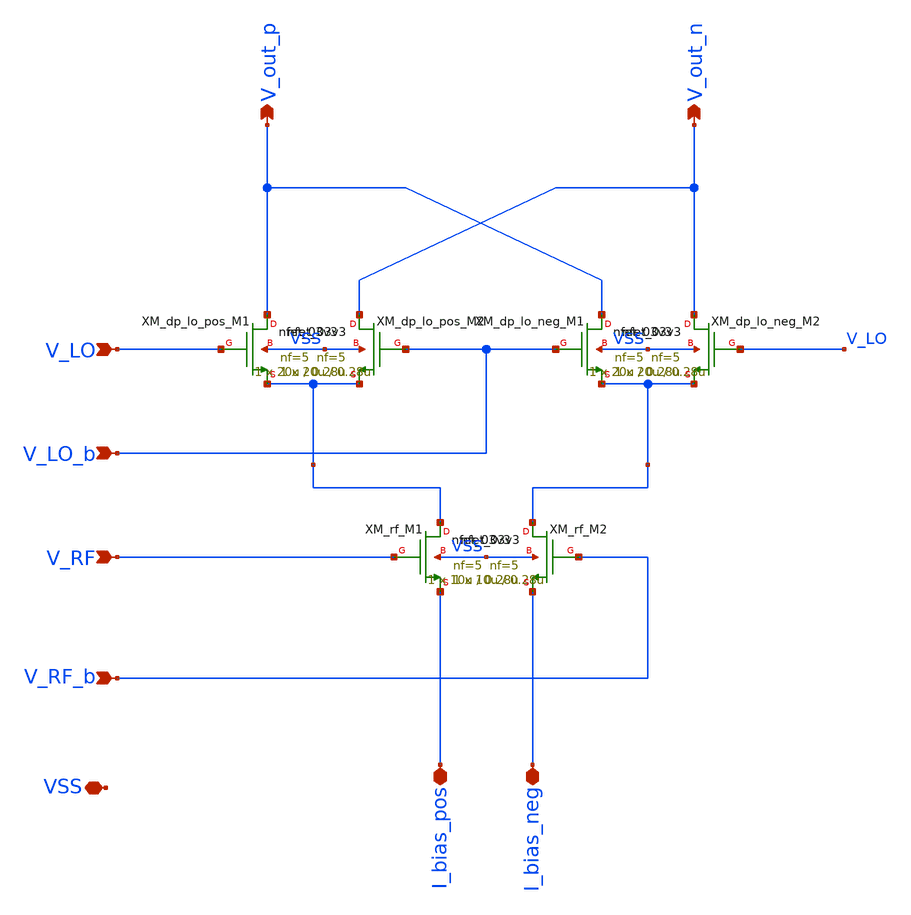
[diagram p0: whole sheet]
** sch_path: src/python/Gilbert_mixer/Gilbert_cell_hierarchal_mixing_stage.sch
**.subckt Gilbert_cell_hierarchal_mixing_stage V_LO V_LO_b V_RF V_RF_b V_out_p V_out_n I_bias_neg
*+ I_bias_pos VSS
*.ipin V_LO
*.ipin V_LO_b
*.ipin V_RF
*.ipin V_RF_b
*.opin V_out_p
*.opin V_out_n
*.iopin I_bias_neg
*.iopin I_bias_pos
*.iopin VSS
XM_dp_lo_pos_M1 V_out_p V_LO rf_diff_pair_pos_input VSS nfet_03v3 L=0.28u W=20u nf=5 ad='int((nf+1)/2) * W/nf * 0.18u'
+ as='int((nf+2)/2) * W/nf * 0.18u' pd='2*int((nf+1)/2) * (W/nf + 0.18u)' ps='2*int((nf+2)/2) * (W/nf + 0.18u)'
+ nrd='0.18u / W' nrs='0.18u / W' sa=0 sb=0 sd=0 m=1
XM_dp_lo_pos_M2 V_out_n V_LO_b rf_diff_pair_pos_input VSS nfet_03v3 L=0.28u W=20u nf=5 ad='int((nf+1)/2) * W/nf * 0.18u'
+ as='int((nf+2)/2) * W/nf * 0.18u' pd='2*int((nf+1)/2) * (W/nf + 0.18u)' ps='2*int((nf+2)/2) * (W/nf + 0.18u)'
+ nrd='0.18u / W' nrs='0.18u / W' sa=0 sb=0 sd=0 m=1
XM_dp_lo_neg_M1 V_out_p V_LO_b rf_diff_pair_neg_input VSS nfet_03v3 L=0.28u W=20u nf=5 ad='int((nf+1)/2) * W/nf * 0.18u'
+ as='int((nf+2)/2) * W/nf * 0.18u' pd='2*int((nf+1)/2) * (W/nf + 0.18u)' ps='2*int((nf+2)/2) * (W/nf + 0.18u)'
+ nrd='0.18u / W' nrs='0.18u / W' sa=0 sb=0 sd=0 m=1
XM_dp_lo_neg_M2 V_out_n V_LO rf_diff_pair_neg_input VSS nfet_03v3 L=0.28u W=20u nf=5 ad='int((nf+1)/2) * W/nf * 0.18u'
+ as='int((nf+2)/2) * W/nf * 0.18u' pd='2*int((nf+1)/2) * (W/nf + 0.18u)' ps='2*int((nf+2)/2) * (W/nf + 0.18u)'
+ nrd='0.18u / W' nrs='0.18u / W' sa=0 sb=0 sd=0 m=1
XM_rf_M1 rf_diff_pair_pos_input V_RF I_bias_pos VSS nfet_03v3 L=0.28u W=10u nf=5 ad='int((nf+1)/2) * W/nf * 0.18u'
+ as='int((nf+2)/2) * W/nf * 0.18u' pd='2*int((nf+1)/2) * (W/nf + 0.18u)' ps='2*int((nf+2)/2) * (W/nf + 0.18u)'
+ nrd='0.18u / W' nrs='0.18u / W' sa=0 sb=0 sd=0 m=1
XM_rf_M2 rf_diff_pair_neg_input V_RF_b I_bias_neg VSS nfet_03v3 L=0.28u W=10u nf=5 ad='int((nf+1)/2) * W/nf * 0.18u'
+ as='int((nf+2)/2) * W/nf * 0.18u' pd='2*int((nf+1)/2) * (W/nf + 0.18u)' ps='2*int((nf+2)/2) * (W/nf + 0.18u)'
+ nrd='0.18u / W' nrs='0.18u / W' sa=0 sb=0 sd=0 m=1
**.ends
.end
